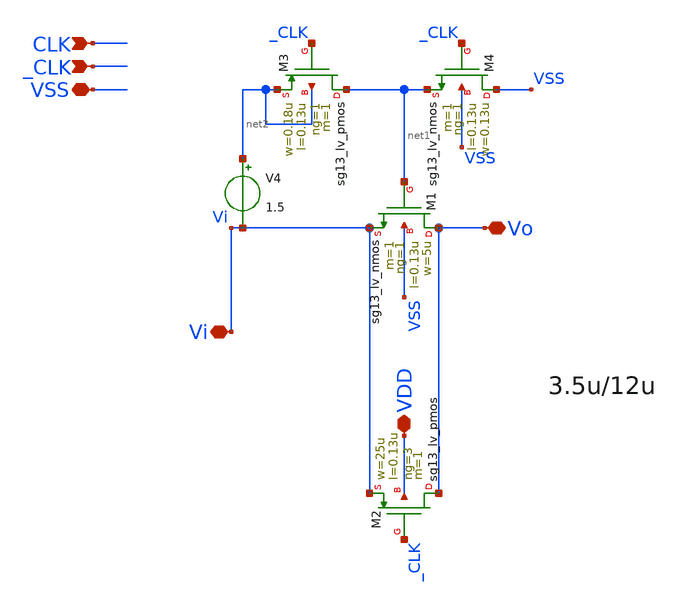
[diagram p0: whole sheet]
** sch_path: sch/blocks/sw_boost.sch
**.subckt sw_boost CLK _CLK Vi Vo VDD VSS
*.ipin CLK
*.ipin _CLK
*.iopin Vi
*.iopin Vo
*.iopin VDD
*.iopin VSS
XM1 Vo net1 Vi VSS sg13_lv_nmos w=5u l=0.13u ng=1 m=1 mm_ok=1
V4 net2 Vi 1.5
XM2 Vo _CLK Vi VDD sg13_lv_pmos w=25u l=0.13u ng=3 m=1 mm_ok=1
XM3 net1 _CLK net2 net2 sg13_lv_pmos w=0.18u l=0.13u ng=1 m=1 mm_ok=1
XM4 VSS _CLK net1 VSS sg13_lv_nmos w=0.13u l=0.13u ng=1 m=1 mm_ok=1
**.ends
.end
